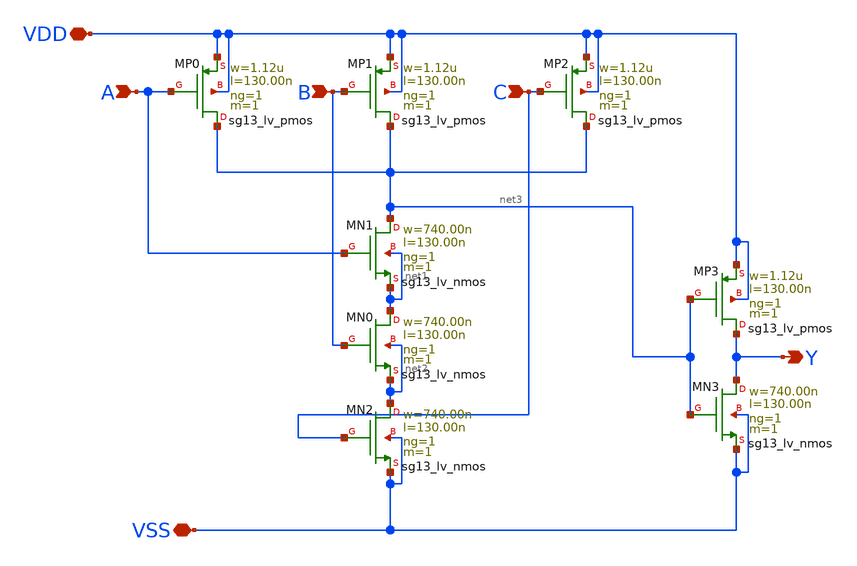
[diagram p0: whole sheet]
** sch_path: xschem/AND3.sch
**.subckt AND3 A VDD VSS B C Y
*.ipin A
*.iopin VDD
*.iopin VSS
*.ipin B
*.ipin C
*.opin Y
XMN0 net1 B net2 net2 sg13_lv_nmos w=740.00n l=130.00n ng=1 m=1 mm_ok=1
XMP0 net3 A VDD VDD sg13_lv_pmos w=1.12u l=130.00n ng=1 m=1 mm_ok=1
XMN1 net3 A net1 net1 sg13_lv_nmos w=740.00n l=130.00n ng=1 m=1 mm_ok=1
XMN2 net2 C VSS VSS sg13_lv_nmos w=740.00n l=130.00n ng=1 m=1 mm_ok=1
XMP1 net3 B VDD VDD sg13_lv_pmos w=1.12u l=130.00n ng=1 m=1 mm_ok=1
XMP2 net3 C VDD VDD sg13_lv_pmos w=1.12u l=130.00n ng=1 m=1 mm_ok=1
XMN3 Y net3 VSS VSS sg13_lv_nmos w=740.00n l=130.00n ng=1 m=1 mm_ok=1
XMP3 Y net3 VDD VDD sg13_lv_pmos w=1.12u l=130.00n ng=1 m=1 mm_ok=1
**.ends
.end
